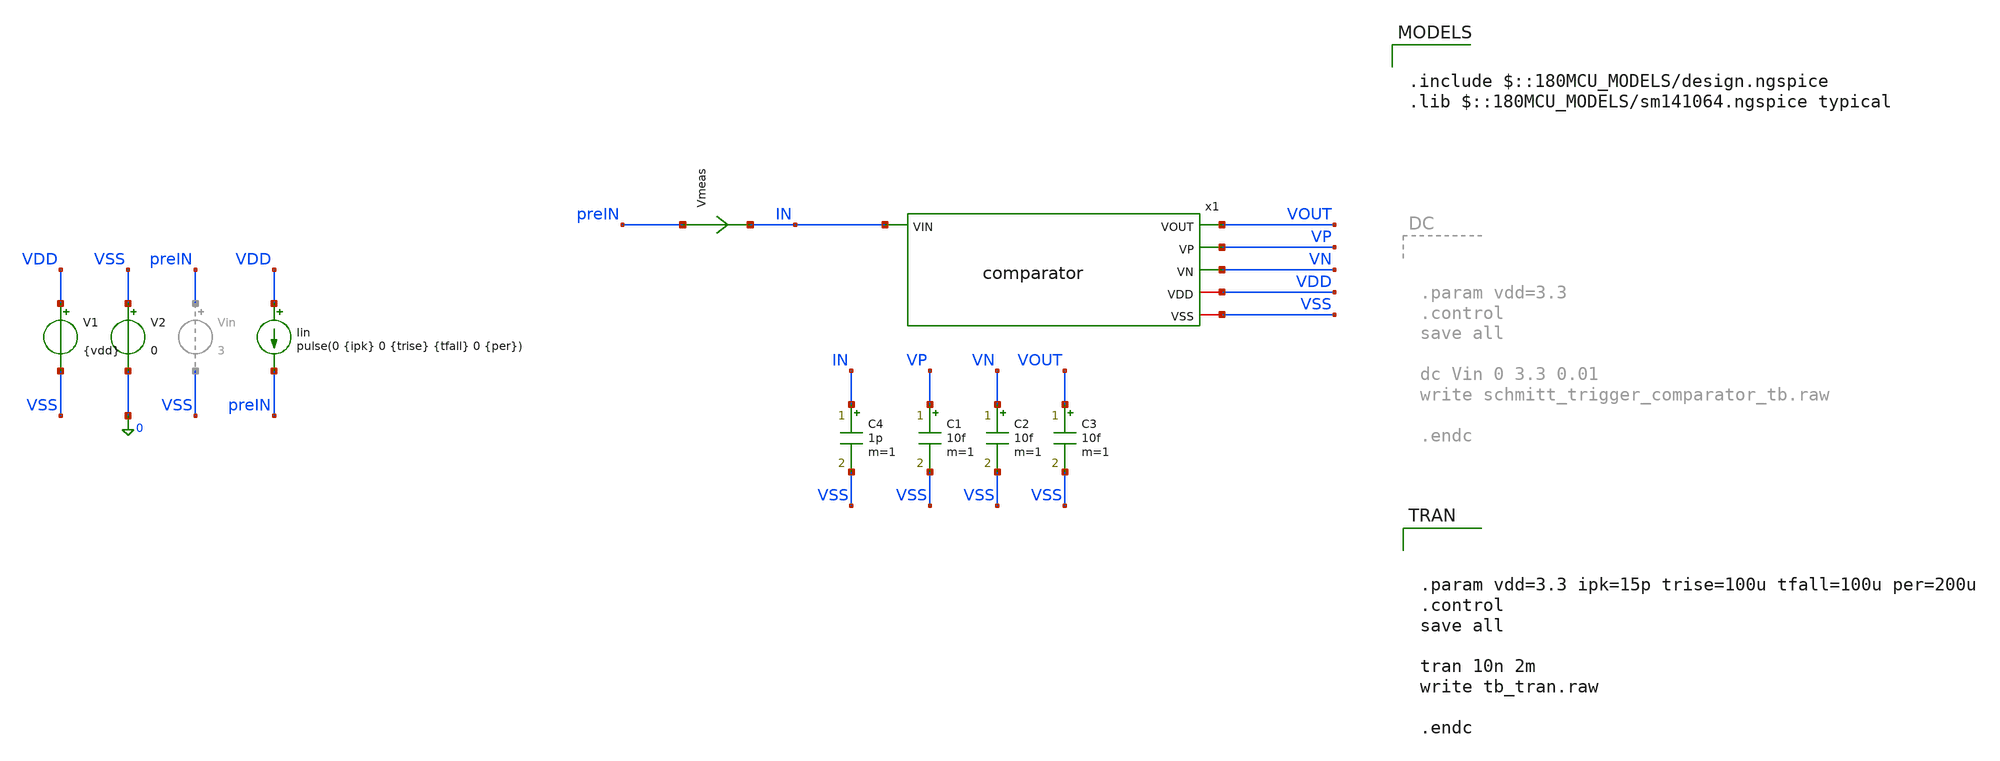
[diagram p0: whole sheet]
** sch_path: analog/neuron/schmitt_trigger_comparator_testbench.sch
**.subckt schmitt_trigger_comparator_testbench
x1 IN VOUT VP VN VDD VSS comparator
V1 VDD VSS {vdd}
V2 VSS 0 0
C1 VP VSS 10f m=1
C2 VN VSS 10f m=1
C3 VOUT VSS 10f m=1
Iin VDD preIN pulse(0 {ipk} 0 {trise} {tfall} 0 {per})
C4 IN VSS 1p m=1
Vmeas preIN IN 0
.save i(vmeas)
**** begin user architecture code

.include $::180MCU_MODELS/design.ngspice
.lib $::180MCU_MODELS/sm141064.ngspice typical




.param vdd=3.3 ipk=15p trise=100u tfall=100u per=200u
.control
save all

tran 10n 2m
write tb_tran.raw

.endc


**** end user architecture code
**.ends
.end
